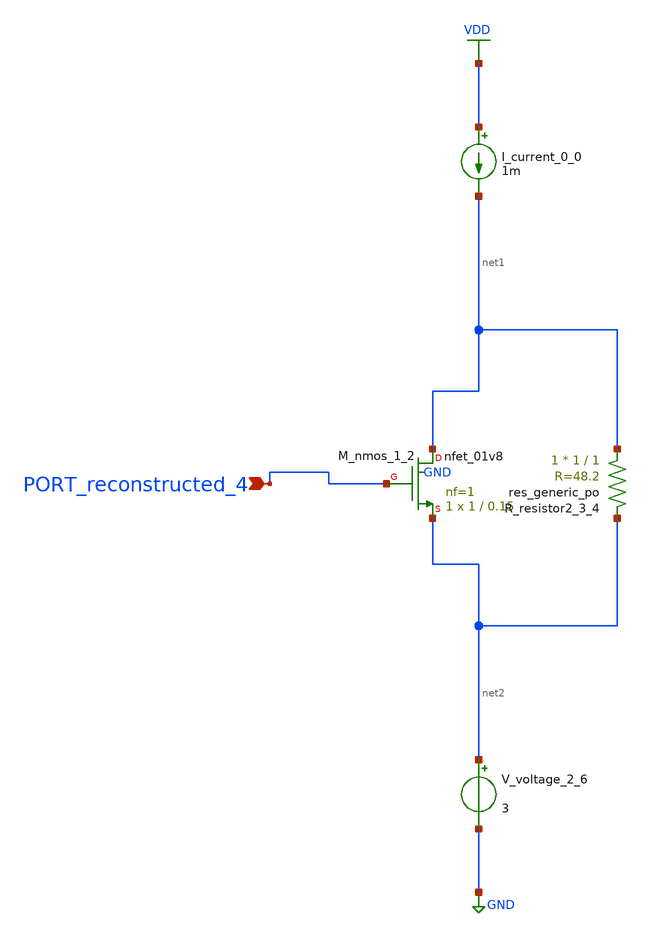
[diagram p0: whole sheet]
** sch_path: schematics/AMSNet/120.sch
**.subckt 120 PORT_reconstructed_4
*.ipin PORT_reconstructed_4
I_current_0_0 VDD net1 1m
XM_nmos_1_2 net1 PORT_reconstructed_4 net2 GND sky130_fd_pr__nfet_01v8 L=0.15 W=1 nf=1 ad='int((1 + 1)/2) * 1 / 1 * 0.29'
+ as='int((1 + 2)/2) * 1 / 1 * 0.29' pd='2*int((1 + 1)/2) * (1 / 1 + 0.29)' ps='2*int((1 + 2)/2) * (1 / 1 + 0.29)'
+ nrd='0.29 / 1 ' nrs='0.29 / 1 ' sa=0 sb=0 sd=0 mult=1 m=1
XR_resistor2_3_4 net1 net2 sky130_fd_pr__res_generic_po W=1 L=1 m=1
V_voltage_2_6 net2 GND 3
**.ends
.GLOBAL GND
.GLOBAL VDD
.end
